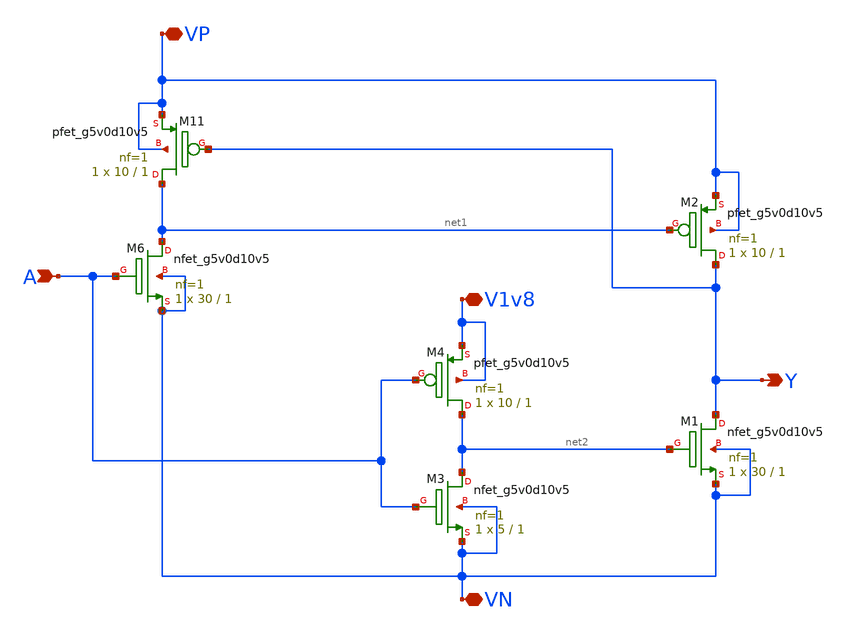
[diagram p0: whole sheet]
** sch_path: ADC/16bit_C2C/MagicAndSpice/shift_1v8_to_5v.sch
**.subckt shift_1v8_to_5v A Y VP VN V1v8
*.ipin A
*.opin Y
*.iopin VP
*.iopin VN
*.iopin V1v8
XM6 net1 A VN VN sky130_fd_pr__nfet_g5v0d10v5 L=1 W=30 nf=1 ad='int((nf+1)/2) * W/nf * 0.29' as='int((nf+2)/2) * W/nf * 0.29'
+ pd='2*int((nf+1)/2) * (W/nf + 0.29)' ps='2*int((nf+2)/2) * (W/nf + 0.29)' nrd='0.29 / W' nrs='0.29 / W'
+ sa=0 sb=0 sd=0 mult=1 m=1
XM11 net1 Y VP VP sky130_fd_pr__pfet_g5v0d10v5 L=1 W=10 nf=1 ad='int((nf+1)/2) * W/nf * 0.29' as='int((nf+2)/2) * W/nf * 0.29'
+ pd='2*int((nf+1)/2) * (W/nf + 0.29)' ps='2*int((nf+2)/2) * (W/nf + 0.29)' nrd='0.29 / W' nrs='0.29 / W'
+ sa=0 sb=0 sd=0 mult=1 m=1
XM1 Y net2 VN VN sky130_fd_pr__nfet_g5v0d10v5 L=1 W=30 nf=1 ad='int((nf+1)/2) * W/nf * 0.29' as='int((nf+2)/2) * W/nf * 0.29'
+ pd='2*int((nf+1)/2) * (W/nf + 0.29)' ps='2*int((nf+2)/2) * (W/nf + 0.29)' nrd='0.29 / W' nrs='0.29 / W'
+ sa=0 sb=0 sd=0 mult=1 m=1
XM2 Y net1 VP VP sky130_fd_pr__pfet_g5v0d10v5 L=1 W=10 nf=1 ad='int((nf+1)/2) * W/nf * 0.29' as='int((nf+2)/2) * W/nf * 0.29'
+ pd='2*int((nf+1)/2) * (W/nf + 0.29)' ps='2*int((nf+2)/2) * (W/nf + 0.29)' nrd='0.29 / W' nrs='0.29 / W'
+ sa=0 sb=0 sd=0 mult=1 m=1
XM3 net2 A VN VN sky130_fd_pr__nfet_g5v0d10v5 L=1 W=5 nf=1 ad='int((nf+1)/2) * W/nf * 0.29' as='int((nf+2)/2) * W/nf * 0.29'
+ pd='2*int((nf+1)/2) * (W/nf + 0.29)' ps='2*int((nf+2)/2) * (W/nf + 0.29)' nrd='0.29 / W' nrs='0.29 / W'
+ sa=0 sb=0 sd=0 mult=1 m=1
XM4 net2 A V1v8 V1v8 sky130_fd_pr__pfet_g5v0d10v5 L=1 W=10 nf=1 ad='int((nf+1)/2) * W/nf * 0.29' as='int((nf+2)/2) * W/nf * 0.29'
+ pd='2*int((nf+1)/2) * (W/nf + 0.29)' ps='2*int((nf+2)/2) * (W/nf + 0.29)' nrd='0.29 / W' nrs='0.29 / W'
+ sa=0 sb=0 sd=0 mult=1 m=1
**.ends
.end
